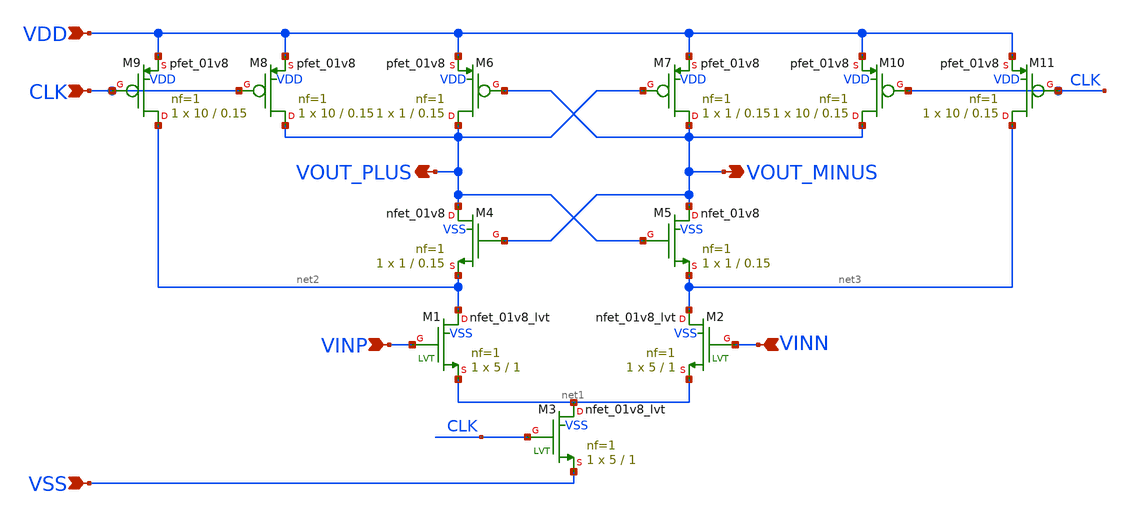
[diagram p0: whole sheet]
** sch_path: xschem/flash_converter/strong_arm_latch.sch
**.subckt strong_arm_latch VSS VDD CLK VINP VINN VOUT_MINUS VOUT_PLUS
*.ipin VSS
*.ipin VDD
*.ipin CLK
*.ipin VINP
*.ipin VINN
*.opin VOUT_MINUS
*.opin VOUT_PLUS
XM1 net2 VINP net1 VSS sky130_fd_pr__nfet_01v8_lvt L=1 W=5 nf=1 ad='int((nf+1)/2) * W/nf * 0.29' as='int((nf+2)/2) * W/nf * 0.29'
+ pd='2*int((nf+1)/2) * (W/nf + 0.29)' ps='2*int((nf+2)/2) * (W/nf + 0.29)' nrd='0.29 / W' nrs='0.29 / W'
+ sa=0 sb=0 sd=0 mult=1 m=1
XM2 net3 VINN net1 VSS sky130_fd_pr__nfet_01v8_lvt L=1 W=5 nf=1 ad='int((nf+1)/2) * W/nf * 0.29' as='int((nf+2)/2) * W/nf * 0.29'
+ pd='2*int((nf+1)/2) * (W/nf + 0.29)' ps='2*int((nf+2)/2) * (W/nf + 0.29)' nrd='0.29 / W' nrs='0.29 / W'
+ sa=0 sb=0 sd=0 mult=1 m=1
XM3 net1 CLK VSS VSS sky130_fd_pr__nfet_01v8_lvt L=1 W=5 nf=1 ad='int((nf+1)/2) * W/nf * 0.29' as='int((nf+2)/2) * W/nf * 0.29'
+ pd='2*int((nf+1)/2) * (W/nf + 0.29)' ps='2*int((nf+2)/2) * (W/nf + 0.29)' nrd='0.29 / W' nrs='0.29 / W'
+ sa=0 sb=0 sd=0 mult=1 m=1
XM4 VOUT_PLUS VOUT_MINUS net2 VSS sky130_fd_pr__nfet_01v8 L=0.15 W=1 nf=1 ad='int((nf+1)/2) * W/nf * 0.29'
+ as='int((nf+2)/2) * W/nf * 0.29' pd='2*int((nf+1)/2) * (W/nf + 0.29)' ps='2*int((nf+2)/2) * (W/nf + 0.29)'
+ nrd='0.29 / W' nrs='0.29 / W' sa=0 sb=0 sd=0 mult=1 m=1
XM5 VOUT_MINUS VOUT_PLUS net3 VSS sky130_fd_pr__nfet_01v8 L=0.15 W=1 nf=1 ad='int((nf+1)/2) * W/nf * 0.29'
+ as='int((nf+2)/2) * W/nf * 0.29' pd='2*int((nf+1)/2) * (W/nf + 0.29)' ps='2*int((nf+2)/2) * (W/nf + 0.29)'
+ nrd='0.29 / W' nrs='0.29 / W' sa=0 sb=0 sd=0 mult=1 m=1
XM6 VOUT_PLUS VOUT_MINUS VDD VDD sky130_fd_pr__pfet_01v8 L=0.15 W=1 nf=1 ad='int((nf+1)/2) * W/nf * 0.29'
+ as='int((nf+2)/2) * W/nf * 0.29' pd='2*int((nf+1)/2) * (W/nf + 0.29)' ps='2*int((nf+2)/2) * (W/nf + 0.29)'
+ nrd='0.29 / W' nrs='0.29 / W' sa=0 sb=0 sd=0 mult=1 m=1
XM7 VOUT_MINUS VOUT_PLUS VDD VDD sky130_fd_pr__pfet_01v8 L=0.15 W=1 nf=1 ad='int((nf+1)/2) * W/nf * 0.29'
+ as='int((nf+2)/2) * W/nf * 0.29' pd='2*int((nf+1)/2) * (W/nf + 0.29)' ps='2*int((nf+2)/2) * (W/nf + 0.29)'
+ nrd='0.29 / W' nrs='0.29 / W' sa=0 sb=0 sd=0 mult=1 m=1
XM8 VOUT_PLUS CLK VDD VDD sky130_fd_pr__pfet_01v8 L=0.15 W=10 nf=1 ad='int((nf+1)/2) * W/nf * 0.29' as='int((nf+2)/2) * W/nf * 0.29'
+ pd='2*int((nf+1)/2) * (W/nf + 0.29)' ps='2*int((nf+2)/2) * (W/nf + 0.29)' nrd='0.29 / W' nrs='0.29 / W'
+ sa=0 sb=0 sd=0 mult=1 m=1
XM9 net2 CLK VDD VDD sky130_fd_pr__pfet_01v8 L=0.15 W=10 nf=1 ad='int((nf+1)/2) * W/nf * 0.29' as='int((nf+2)/2) * W/nf * 0.29'
+ pd='2*int((nf+1)/2) * (W/nf + 0.29)' ps='2*int((nf+2)/2) * (W/nf + 0.29)' nrd='0.29 / W' nrs='0.29 / W'
+ sa=0 sb=0 sd=0 mult=1 m=1
XM10 VOUT_MINUS CLK VDD VDD sky130_fd_pr__pfet_01v8 L=0.15 W=10 nf=1 ad='int((nf+1)/2) * W/nf * 0.29'
+ as='int((nf+2)/2) * W/nf * 0.29' pd='2*int((nf+1)/2) * (W/nf + 0.29)' ps='2*int((nf+2)/2) * (W/nf + 0.29)'
+ nrd='0.29 / W' nrs='0.29 / W' sa=0 sb=0 sd=0 mult=1 m=1
XM11 net3 CLK VDD VDD sky130_fd_pr__pfet_01v8 L=0.15 W=10 nf=1 ad='int((nf+1)/2) * W/nf * 0.29' as='int((nf+2)/2) * W/nf * 0.29'
+ pd='2*int((nf+1)/2) * (W/nf + 0.29)' ps='2*int((nf+2)/2) * (W/nf + 0.29)' nrd='0.29 / W' nrs='0.29 / W'
+ sa=0 sb=0 sd=0 mult=1 m=1
**.ends
.end
